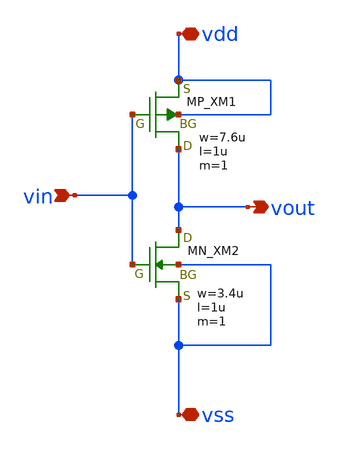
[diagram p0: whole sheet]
** sch_path: inverter.sch
**.subckt inverter vdd vout vss vin
*.iopin vdd
*.opin vout
*.iopin vss
*.ipin vin
XXM1 vout vin vdd vdd PMOS w=7.6u l=1u nrd=0 nrs=0 m=1
XXM2 vout vin vss vss NMOS w=3.4u l=1u nrd=0 nrs=0 m=1
**.ends
.end
